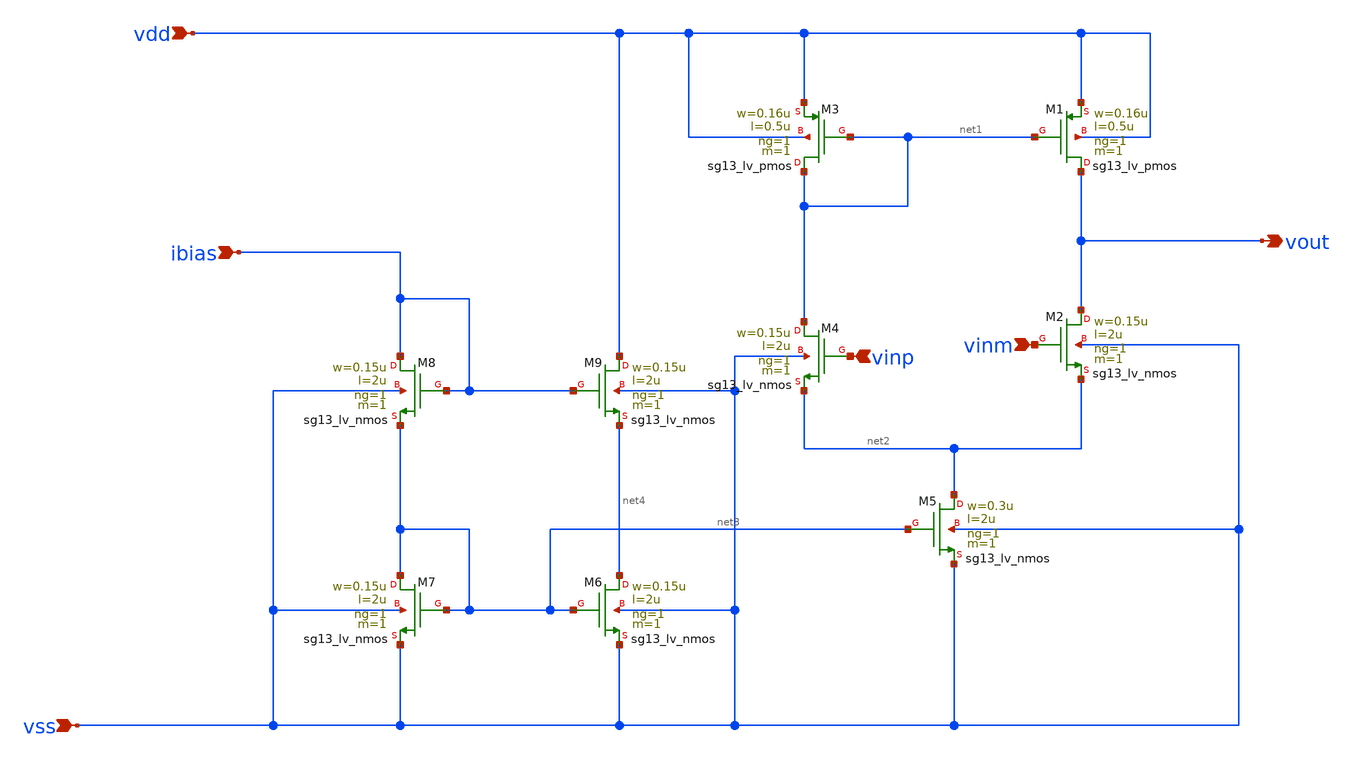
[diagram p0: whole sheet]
** sch_path: zip_meiners/ic_design/design_switch_cap/basic_5t_ota_switchcap.sch
**.subckt basic_5t_ota_switchcap vss vdd ibias vinm vinp vout
*.ipin vss
*.ipin vdd
*.ipin ibias
*.ipin vinm
*.ipin vinp
*.opin vout
XM1 vout net1 vdd vdd sg13_lv_pmos w=0.16u l=0.5u ng=1 m=1 mm_ok=1
XM2 vout vinm net2 vss sg13_lv_nmos w=0.15u l=2u ng=1 m=1 mm_ok=1
XM3 net1 net1 vdd vdd sg13_lv_pmos w=0.16u l=0.5u ng=1 m=1 mm_ok=1
XM4 net1 vinp net2 vss sg13_lv_nmos w=0.15u l=2u ng=1 m=1 mm_ok=1
XM5 net2 net3 vss vss sg13_lv_nmos w=0.3u l=2u ng=1 m=1 mm_ok=1
XM6 net4 net3 vss vss sg13_lv_nmos w=0.15u l=2u ng=1 m=1 mm_ok=1
XM7 net3 net3 vss vss sg13_lv_nmos w=0.15u l=2u ng=1 m=1 mm_ok=1
XM9 vdd ibias net4 vss sg13_lv_nmos w=0.15u l=2u ng=1 m=1 mm_ok=1
XM8 ibias ibias net3 vss sg13_lv_nmos w=0.15u l=2u ng=1 m=1 mm_ok=1
**.ends
.end
